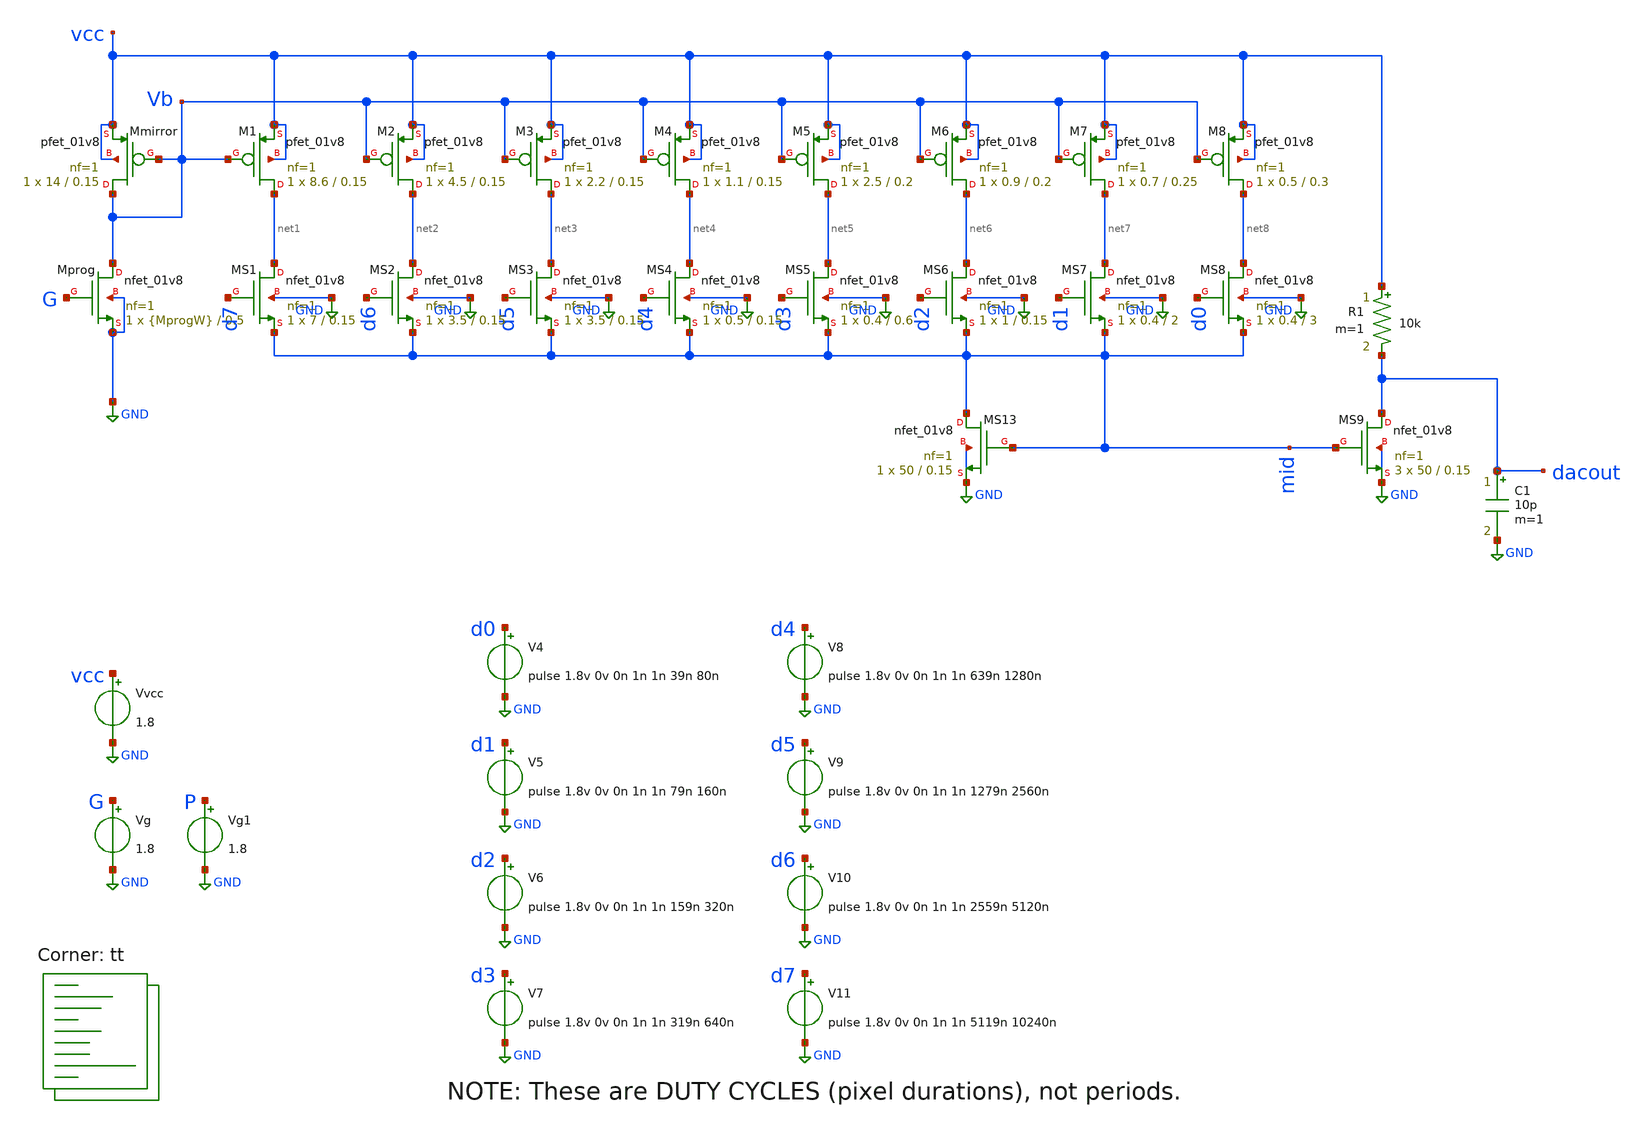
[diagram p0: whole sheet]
** sch_path: xschem/06-csdac3.sch
**.subckt 06-csdac3
Vvcc vcc GND 1.8
Vg G GND 1.8
XMprog Vb G GND GND sky130_fd_pr__nfet_01v8 L=0.5 W={MprogW} nf=1 ad='int((nf+1)/2) * W/nf * 0.29' as='int((nf+2)/2) * W/nf * 0.29'
+ pd='2*int((nf+1)/2) * (W/nf + 0.29)' ps='2*int((nf+2)/2) * (W/nf + 0.29)' nrd='0.29 / W' nrs='0.29 / W'
+ sa=0 sb=0 sd=0 mult=1 m=1
XMmirror Vb Vb vcc vcc sky130_fd_pr__pfet_01v8 L=0.15 W=14 nf=1 ad='int((nf+1)/2) * W/nf * 0.29' as='int((nf+2)/2) * W/nf * 0.29'
+ pd='2*int((nf+1)/2) * (W/nf + 0.29)' ps='2*int((nf+2)/2) * (W/nf + 0.29)' nrd='0.29 / W' nrs='0.29 / W'
+ sa=0 sb=0 sd=0 mult=1 m=1
XM1 net1 Vb vcc vcc sky130_fd_pr__pfet_01v8 L=0.15 W=8.6 nf=1 ad='int((nf+1)/2) * W/nf * 0.29' as='int((nf+2)/2) * W/nf * 0.29'
+ pd='2*int((nf+1)/2) * (W/nf + 0.29)' ps='2*int((nf+2)/2) * (W/nf + 0.29)' nrd='0.29 / W' nrs='0.29 / W'
+ sa=0 sb=0 sd=0 mult=1 m=1
XM2 net2 Vb vcc vcc sky130_fd_pr__pfet_01v8 L=0.15 W=4.5 nf=1 ad='int((nf+1)/2) * W/nf * 0.29' as='int((nf+2)/2) * W/nf * 0.29'
+ pd='2*int((nf+1)/2) * (W/nf + 0.29)' ps='2*int((nf+2)/2) * (W/nf + 0.29)' nrd='0.29 / W' nrs='0.29 / W'
+ sa=0 sb=0 sd=0 mult=1 m=1
XM3 net3 Vb vcc vcc sky130_fd_pr__pfet_01v8 L=0.15 W=2.2 nf=1 ad='int((nf+1)/2) * W/nf * 0.29' as='int((nf+2)/2) * W/nf * 0.29'
+ pd='2*int((nf+1)/2) * (W/nf + 0.29)' ps='2*int((nf+2)/2) * (W/nf + 0.29)' nrd='0.29 / W' nrs='0.29 / W'
+ sa=0 sb=0 sd=0 mult=1 m=1
XM4 net4 Vb vcc vcc sky130_fd_pr__pfet_01v8 L=0.15 W=1.1 nf=1 ad='int((nf+1)/2) * W/nf * 0.29' as='int((nf+2)/2) * W/nf * 0.29'
+ pd='2*int((nf+1)/2) * (W/nf + 0.29)' ps='2*int((nf+2)/2) * (W/nf + 0.29)' nrd='0.29 / W' nrs='0.29 / W'
+ sa=0 sb=0 sd=0 mult=1 m=1
XM5 net5 Vb vcc vcc sky130_fd_pr__pfet_01v8 L=0.2 W=2.5 nf=1 ad='int((nf+1)/2) * W/nf * 0.29' as='int((nf+2)/2) * W/nf * 0.29'
+ pd='2*int((nf+1)/2) * (W/nf + 0.29)' ps='2*int((nf+2)/2) * (W/nf + 0.29)' nrd='0.29 / W' nrs='0.29 / W'
+ sa=0 sb=0 sd=0 mult=1 m=1
XM6 net6 Vb vcc vcc sky130_fd_pr__pfet_01v8 L=0.2 W=0.9 nf=1 ad='int((nf+1)/2) * W/nf * 0.29' as='int((nf+2)/2) * W/nf * 0.29'
+ pd='2*int((nf+1)/2) * (W/nf + 0.29)' ps='2*int((nf+2)/2) * (W/nf + 0.29)' nrd='0.29 / W' nrs='0.29 / W'
+ sa=0 sb=0 sd=0 mult=1 m=1
XM7 net7 Vb vcc vcc sky130_fd_pr__pfet_01v8 L=0.25 W=0.7 nf=1 ad='int((nf+1)/2) * W/nf * 0.29' as='int((nf+2)/2) * W/nf * 0.29'
+ pd='2*int((nf+1)/2) * (W/nf + 0.29)' ps='2*int((nf+2)/2) * (W/nf + 0.29)' nrd='0.29 / W' nrs='0.29 / W'
+ sa=0 sb=0 sd=0 mult=1 m=1
XM8 net8 Vb vcc vcc sky130_fd_pr__pfet_01v8 L=0.3 W=0.5 nf=1 ad='int((nf+1)/2) * W/nf * 0.29' as='int((nf+2)/2) * W/nf * 0.29'
+ pd='2*int((nf+1)/2) * (W/nf + 0.29)' ps='2*int((nf+2)/2) * (W/nf + 0.29)' nrd='0.29 / W' nrs='0.29 / W'
+ sa=0 sb=0 sd=0 mult=1 m=1
XMS1 net1 d7 mid GND sky130_fd_pr__nfet_01v8 L=0.15 W=7 nf=1 ad='int((nf+1)/2) * W/nf * 0.29' as='int((nf+2)/2) * W/nf * 0.29'
+ pd='2*int((nf+1)/2) * (W/nf + 0.29)' ps='2*int((nf+2)/2) * (W/nf + 0.29)' nrd='0.29 / W' nrs='0.29 / W'
+ sa=0 sb=0 sd=0 mult=1 m=1
XMS2 net2 d6 mid GND sky130_fd_pr__nfet_01v8 L=0.15 W=3.5 nf=1 ad='int((nf+1)/2) * W/nf * 0.29' as='int((nf+2)/2) * W/nf * 0.29'
+ pd='2*int((nf+1)/2) * (W/nf + 0.29)' ps='2*int((nf+2)/2) * (W/nf + 0.29)' nrd='0.29 / W' nrs='0.29 / W'
+ sa=0 sb=0 sd=0 mult=1 m=1
XMS3 net3 d5 mid GND sky130_fd_pr__nfet_01v8 L=0.15 W=3.5 nf=1 ad='int((nf+1)/2) * W/nf * 0.29' as='int((nf+2)/2) * W/nf * 0.29'
+ pd='2*int((nf+1)/2) * (W/nf + 0.29)' ps='2*int((nf+2)/2) * (W/nf + 0.29)' nrd='0.29 / W' nrs='0.29 / W'
+ sa=0 sb=0 sd=0 mult=1 m=1
XMS4 net4 d4 mid GND sky130_fd_pr__nfet_01v8 L=0.15 W=0.5 nf=1 ad='int((nf+1)/2) * W/nf * 0.29' as='int((nf+2)/2) * W/nf * 0.29'
+ pd='2*int((nf+1)/2) * (W/nf + 0.29)' ps='2*int((nf+2)/2) * (W/nf + 0.29)' nrd='0.29 / W' nrs='0.29 / W'
+ sa=0 sb=0 sd=0 mult=1 m=1
XMS5 net5 d3 mid GND sky130_fd_pr__nfet_01v8 L=0.6 W=0.4 nf=1 ad='int((nf+1)/2) * W/nf * 0.29' as='int((nf+2)/2) * W/nf * 0.29'
+ pd='2*int((nf+1)/2) * (W/nf + 0.29)' ps='2*int((nf+2)/2) * (W/nf + 0.29)' nrd='0.29 / W' nrs='0.29 / W'
+ sa=0 sb=0 sd=0 mult=1 m=1
XMS6 net6 d2 mid GND sky130_fd_pr__nfet_01v8 L=0.15 W=1 nf=1 ad='int((nf+1)/2) * W/nf * 0.29' as='int((nf+2)/2) * W/nf * 0.29'
+ pd='2*int((nf+1)/2) * (W/nf + 0.29)' ps='2*int((nf+2)/2) * (W/nf + 0.29)' nrd='0.29 / W' nrs='0.29 / W'
+ sa=0 sb=0 sd=0 mult=1 m=1
XMS7 net7 d1 mid GND sky130_fd_pr__nfet_01v8 L=2 W=0.4 nf=1 ad='int((nf+1)/2) * W/nf * 0.29' as='int((nf+2)/2) * W/nf * 0.29'
+ pd='2*int((nf+1)/2) * (W/nf + 0.29)' ps='2*int((nf+2)/2) * (W/nf + 0.29)' nrd='0.29 / W' nrs='0.29 / W'
+ sa=0 sb=0 sd=0 mult=1 m=1
XMS8 net8 d0 mid GND sky130_fd_pr__nfet_01v8 L=3 W=0.4 nf=1 ad='int((nf+1)/2) * W/nf * 0.29' as='int((nf+2)/2) * W/nf * 0.29'
+ pd='2*int((nf+1)/2) * (W/nf + 0.29)' ps='2*int((nf+2)/2) * (W/nf + 0.29)' nrd='0.29 / W' nrs='0.29 / W'
+ sa=0 sb=0 sd=0 mult=1 m=1
V4 d0 GND pulse 1.8v 0v 0n 1n 1n 39n 80n
V5 d1 GND pulse 1.8v 0v 0n 1n 1n 79n 160n
V6 d2 GND pulse 1.8v 0v 0n 1n 1n 159n 320n
V7 d3 GND pulse 1.8v 0v 0n 1n 1n 319n 640n
V8 d4 GND pulse 1.8v 0v 0n 1n 1n 639n 1280n
V9 d5 GND pulse 1.8v 0v 0n 1n 1n 1279n 2560n
V10 d6 GND pulse 1.8v 0v 0n 1n 1n 2559n 5120n
V11 d7 GND pulse 1.8v 0v 0n 1n 1n 5119n 10240n
Vg1 P GND 1.8
C1 dacout GND 10p m=1
XMS13 mid mid GND GND sky130_fd_pr__nfet_01v8 L=0.15 W=50 nf=1 ad='int((nf+1)/2) * W/nf * 0.29' as='int((nf+2)/2) * W/nf * 0.29'
+ pd='2*int((nf+1)/2) * (W/nf + 0.29)' ps='2*int((nf+2)/2) * (W/nf + 0.29)' nrd='0.29 / W' nrs='0.29 / W'
+ sa=0 sb=0 sd=0 mult=1 m=1
XMS9 dacout mid GND GND sky130_fd_pr__nfet_01v8 L=0.15 W=50 nf=1 ad='int((nf+1)/2) * W/nf * 0.29' as='int((nf+2)/2) * W/nf * 0.29'
+ pd='2*int((nf+1)/2) * (W/nf + 0.29)' ps='2*int((nf+2)/2) * (W/nf + 0.29)' nrd='0.29 / W' nrs='0.29 / W'
+ sa=0 sb=0 sd=0 mult=3 m=3
R1 vcc dacout 10k m=1
**** begin user architecture code



.param MprogW=1
.options savecurrents
.control

*  set temp=90
  save all
  tran 1n 12.8u
  write 06.raw v(mid) v(dacout) v(Vb)

*  set appendwrite
*  alterparam MprogW=0.9
*  reset
**  *set temp=10
*  tran 1n 12.8u
*  write 05.raw
** v(dacout)

.endc



.lib $::SKYWATER_MODELS/sky130.lib.spice tt
**** end user architecture code
**.ends
.GLOBAL GND
.end
